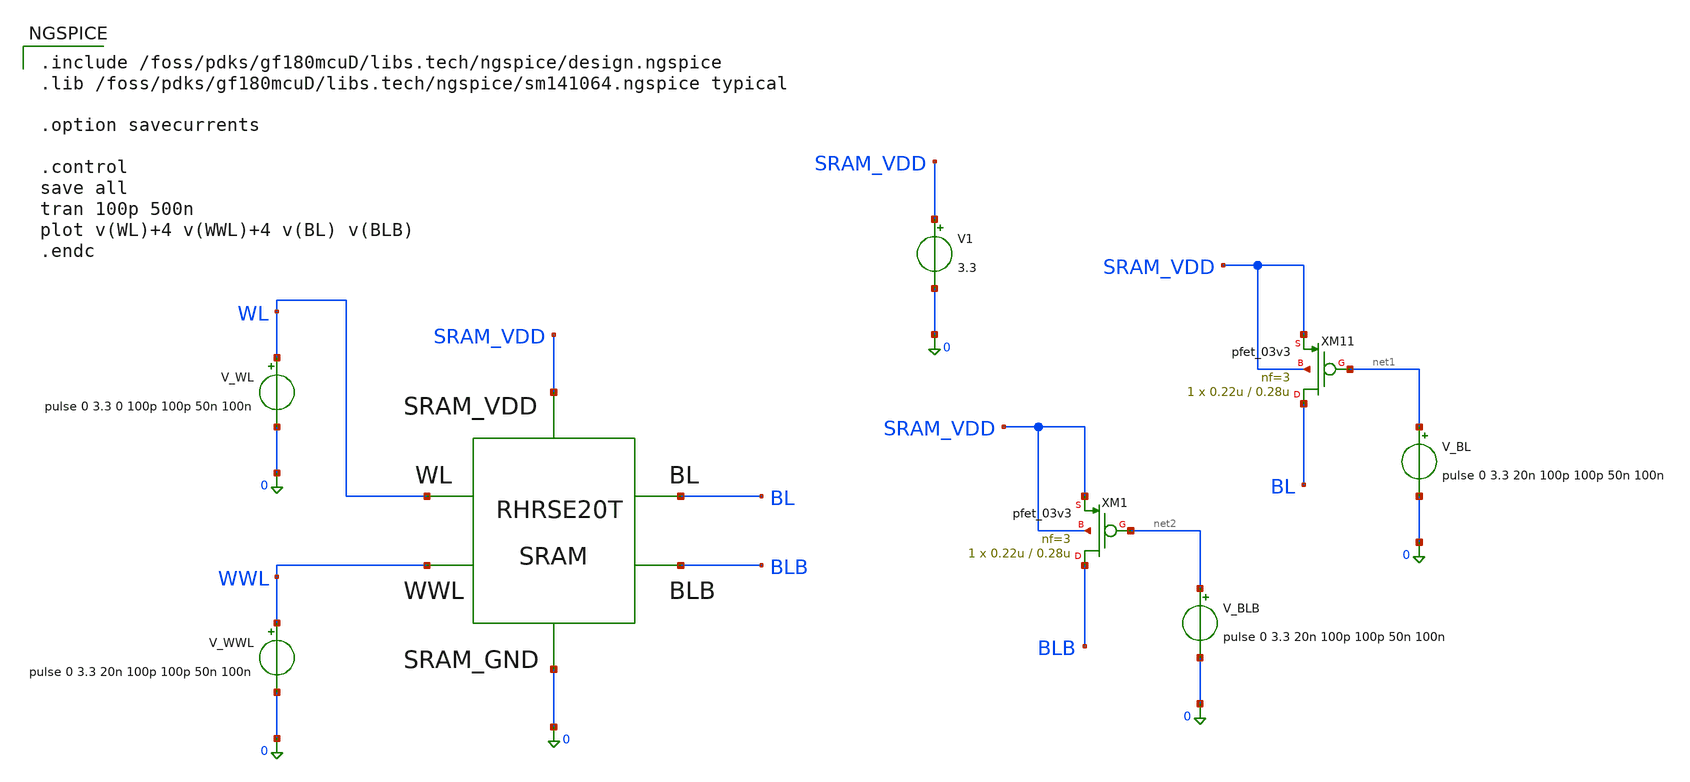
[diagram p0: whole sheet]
** sch_path: bitcell/RHRSE20T_transient_simulation_without_radiation.sch
**.subckt RHRSE20T_transient_simulation_without_radiation
XM11 BL net1 SRAM_VDD SRAM_VDD pfet_03v3 L=0.28u W=0.22u nf=3 ad='int((nf+1)/2) * W/nf * 0.18u' as='int((nf+2)/2) * W/nf * 0.18u'
+ pd='2*int((nf+1)/2) * (W/nf + 0.18u)' ps='2*int((nf+2)/2) * (W/nf + 0.18u)' nrd='0.18u / W' nrs='0.18u / W'
+ sa=0 sb=0 sd=0 m=1
x1 0 BL BLB SRAM_VDD WL WWL RHRSE20T
V1 SRAM_VDD 0 3.3
V_WWL WWL 0 pulse 0 3.3 20n 100p 100p 50n 100n
V_WL WL 0 pulse 0 3.3 0 100p 100p 50n 100n
.save i(v_wl)
XM1 BLB net2 SRAM_VDD SRAM_VDD pfet_03v3 L=0.28u W=0.22u nf=3 ad='int((nf+1)/2) * W/nf * 0.18u' as='int((nf+2)/2) * W/nf * 0.18u'
+ pd='2*int((nf+1)/2) * (W/nf + 0.18u)' ps='2*int((nf+2)/2) * (W/nf + 0.18u)' nrd='0.18u / W' nrs='0.18u / W'
+ sa=0 sb=0 sd=0 m=1
V_BLB net2 0 pulse 0 3.3 20n 100p 100p 50n 100n
V_BL net1 0 pulse 0 3.3 20n 100p 100p 50n 100n
**** begin user architecture code

.include /foss/pdks/gf180mcuD/libs.tech/ngspice/design.ngspice
.lib /foss/pdks/gf180mcuD/libs.tech/ngspice/sm141064.ngspice typical

.option savecurrents

.control
save all
tran 100p 500n
plot v(WL)+4 v(WWL)+4 v(BL) v(BLB)
.endc

**** end user architecture code
**.ends

* expanding   symbol:  SRAM/RHRSE20T.sym # of pins=6
** sym_path: bitcell/RHRSE20T.sym
** sch_path: bitcell/RHRSE20T.sch
.subckt RHRSE20T SRAM_GND BL BLB SRAM_VDD WL WWL
*.ipin WWL
*.ipin WL
*.iopin SRAM_VDD
*.iopin SRAM_GND
*.iopin BL
*.iopin BLB
XM1 S0 S3 SRAM_VDD SRAM_VDD pfet_03v3 L=0.28u W=0.22u nf=1 ad='int((nf+1)/2) * W/nf * 0.18u' as='int((nf+2)/2) * W/nf * 0.18u'
+ pd='2*int((nf+1)/2) * (W/nf + 0.18u)' ps='2*int((nf+2)/2) * (W/nf + 0.18u)' nrd='0.18u / W' nrs='0.18u / W'
+ sa=0 sb=0 sd=0 m=1
XM2 net1 S2 SRAM_VDD SRAM_VDD pfet_03v3 L=0.28u W=0.22u nf=1 ad='int((nf+1)/2) * W/nf * 0.18u' as='int((nf+2)/2) * W/nf * 0.18u'
+ pd='2*int((nf+1)/2) * (W/nf + 0.18u)' ps='2*int((nf+2)/2) * (W/nf + 0.18u)' nrd='0.18u / W' nrs='0.18u / W'
+ sa=0 sb=0 sd=0 m=1
XM3 net1 S3 S1 SRAM_GND nfet_03v3 L=0.28u W=0.22u nf=2 ad='int((nf+1)/2) * W/nf * 0.18u' as='int((nf+2)/2) * W/nf * 0.18u'
+ pd='2*int((nf+1)/2) * (W/nf + 0.18u)' ps='2*int((nf+2)/2) * (W/nf + 0.18u)' nrd='0.18u / W' nrs='0.18u / W'
+ sa=0 sb=0 sd=0 m=1
XM4 Q_bar S3 SRAM_GND SRAM_GND nfet_03v3 L=0.28u W=0.22u nf=3 ad='int((nf+1)/2) * W/nf * 0.18u' as='int((nf+2)/2) * W/nf * 0.18u'
+ pd='2*int((nf+1)/2) * (W/nf + 0.18u)' ps='2*int((nf+2)/2) * (W/nf + 0.18u)' nrd='0.18u / W' nrs='0.18u / W'
+ sa=0 sb=0 sd=0 m=1
XM5 Q_bar Q SRAM_VDD SRAM_VDD pfet_03v3 L=0.28u W=0.22u nf=1 ad='int((nf+1)/2) * W/nf * 0.18u' as='int((nf+2)/2) * W/nf * 0.18u'
+ pd='2*int((nf+1)/2) * (W/nf + 0.18u)' ps='2*int((nf+2)/2) * (W/nf + 0.18u)' nrd='0.18u / W' nrs='0.18u / W'
+ sa=0 sb=0 sd=0 m=1
XM6 Q Q_bar SRAM_VDD SRAM_VDD pfet_03v3 L=0.28u W=0.22u nf=1 ad='int((nf+1)/2) * W/nf * 0.18u' as='int((nf+2)/2) * W/nf * 0.18u'
+ pd='2*int((nf+1)/2) * (W/nf + 0.18u)' ps='2*int((nf+2)/2) * (W/nf + 0.18u)' nrd='0.18u / W' nrs='0.18u / W'
+ sa=0 sb=0 sd=0 m=1
XM7 Q S0 SRAM_GND SRAM_GND nfet_03v3 L=0.28u W=0.22u nf=3 ad='int((nf+1)/2) * W/nf * 0.18u' as='int((nf+2)/2) * W/nf * 0.18u'
+ pd='2*int((nf+1)/2) * (W/nf + 0.18u)' ps='2*int((nf+2)/2) * (W/nf + 0.18u)' nrd='0.18u / W' nrs='0.18u / W'
+ sa=0 sb=0 sd=0 m=1
XM8 S1 S2 SRAM_GND SRAM_GND nfet_03v3 L=0.28u W=0.22u nf=2 ad='int((nf+1)/2) * W/nf * 0.18u' as='int((nf+2)/2) * W/nf * 0.18u'
+ pd='2*int((nf+1)/2) * (W/nf + 0.18u)' ps='2*int((nf+2)/2) * (W/nf + 0.18u)' nrd='0.18u / W' nrs='0.18u / W'
+ sa=0 sb=0 sd=0 m=1
XM9 S0 S1 SRAM_GND SRAM_GND nfet_03v3 L=0.28u W=0.22u nf=2 ad='int((nf+1)/2) * W/nf * 0.18u' as='int((nf+2)/2) * W/nf * 0.18u'
+ pd='2*int((nf+1)/2) * (W/nf + 0.18u)' ps='2*int((nf+2)/2) * (W/nf + 0.18u)' nrd='0.18u / W' nrs='0.18u / W'
+ sa=0 sb=0 sd=0 m=1
XM10 S3 S0 SRAM_VDD SRAM_VDD pfet_03v3 L=0.28u W=0.22u nf=1 ad='int((nf+1)/2) * W/nf * 0.18u' as='int((nf+2)/2) * W/nf * 0.18u'
+ pd='2*int((nf+1)/2) * (W/nf + 0.18u)' ps='2*int((nf+2)/2) * (W/nf + 0.18u)' nrd='0.18u / W' nrs='0.18u / W'
+ sa=0 sb=0 sd=0 m=1
XM11 net2 S1 SRAM_VDD SRAM_VDD pfet_03v3 L=0.28u W=0.22u nf=1 ad='int((nf+1)/2) * W/nf * 0.18u' as='int((nf+2)/2) * W/nf * 0.18u'
+ pd='2*int((nf+1)/2) * (W/nf + 0.18u)' ps='2*int((nf+2)/2) * (W/nf + 0.18u)' nrd='0.18u / W' nrs='0.18u / W'
+ sa=0 sb=0 sd=0 m=1
XM12 net2 S0 S2 SRAM_GND nfet_03v3 L=0.28u W=0.22u nf=2 ad='int((nf+1)/2) * W/nf * 0.18u' as='int((nf+2)/2) * W/nf * 0.18u'
+ pd='2*int((nf+1)/2) * (W/nf + 0.18u)' ps='2*int((nf+2)/2) * (W/nf + 0.18u)' nrd='0.18u / W' nrs='0.18u / W'
+ sa=0 sb=0 sd=0 m=1
XM13 S2 S1 SRAM_GND SRAM_GND nfet_03v3 L=0.28u W=0.22u nf=2 ad='int((nf+1)/2) * W/nf * 0.18u' as='int((nf+2)/2) * W/nf * 0.18u'
+ pd='2*int((nf+1)/2) * (W/nf + 0.18u)' ps='2*int((nf+2)/2) * (W/nf + 0.18u)' nrd='0.18u / W' nrs='0.18u / W'
+ sa=0 sb=0 sd=0 m=1
XM14 S3 S2 SRAM_GND SRAM_GND nfet_03v3 L=0.28u W=0.22u nf=2 ad='int((nf+1)/2) * W/nf * 0.18u' as='int((nf+2)/2) * W/nf * 0.18u'
+ pd='2*int((nf+1)/2) * (W/nf + 0.18u)' ps='2*int((nf+2)/2) * (W/nf + 0.18u)' nrd='0.18u / W' nrs='0.18u / W'
+ sa=0 sb=0 sd=0 m=1
XM15 Q WWL BL SRAM_GND nfet_03v3 L=0.28u W=0.22u nf=2 ad='int((nf+1)/2) * W/nf * 0.18u' as='int((nf+2)/2) * W/nf * 0.18u'
+ pd='2*int((nf+1)/2) * (W/nf + 0.18u)' ps='2*int((nf+2)/2) * (W/nf + 0.18u)' nrd='0.18u / W' nrs='0.18u / W'
+ sa=0 sb=0 sd=0 m=1
XM16 Q_bar WWL BLB SRAM_GND nfet_03v3 L=0.28u W=0.22u nf=2 ad='int((nf+1)/2) * W/nf * 0.18u' as='int((nf+2)/2) * W/nf * 0.18u'
+ pd='2*int((nf+1)/2) * (W/nf + 0.18u)' ps='2*int((nf+2)/2) * (W/nf + 0.18u)' nrd='0.18u / W' nrs='0.18u / W'
+ sa=0 sb=0 sd=0 m=1
XM17 S0 WL BLB SRAM_GND nfet_03v3 L=0.28u W=0.22u nf=2 ad='int((nf+1)/2) * W/nf * 0.18u' as='int((nf+2)/2) * W/nf * 0.18u'
+ pd='2*int((nf+1)/2) * (W/nf + 0.18u)' ps='2*int((nf+2)/2) * (W/nf + 0.18u)' nrd='0.18u / W' nrs='0.18u / W'
+ sa=0 sb=0 sd=0 m=1
XM18 S1 WL BL SRAM_GND nfet_03v3 L=0.28u W=0.22u nf=2 ad='int((nf+1)/2) * W/nf * 0.18u' as='int((nf+2)/2) * W/nf * 0.18u'
+ pd='2*int((nf+1)/2) * (W/nf + 0.18u)' ps='2*int((nf+2)/2) * (W/nf + 0.18u)' nrd='0.18u / W' nrs='0.18u / W'
+ sa=0 sb=0 sd=0 m=1
XM19 S2 WL BLB SRAM_GND nfet_03v3 L=0.28u W=0.22u nf=2 ad='int((nf+1)/2) * W/nf * 0.18u' as='int((nf+2)/2) * W/nf * 0.18u'
+ pd='2*int((nf+1)/2) * (W/nf + 0.18u)' ps='2*int((nf+2)/2) * (W/nf + 0.18u)' nrd='0.18u / W' nrs='0.18u / W'
+ sa=0 sb=0 sd=0 m=1
XM20 S3 WL BL SRAM_GND nfet_03v3 L=0.28u W=0.22u nf=2 ad='int((nf+1)/2) * W/nf * 0.18u' as='int((nf+2)/2) * W/nf * 0.18u'
+ pd='2*int((nf+1)/2) * (W/nf + 0.18u)' ps='2*int((nf+2)/2) * (W/nf + 0.18u)' nrd='0.18u / W' nrs='0.18u / W'
+ sa=0 sb=0 sd=0 m=1
.ends

.end
